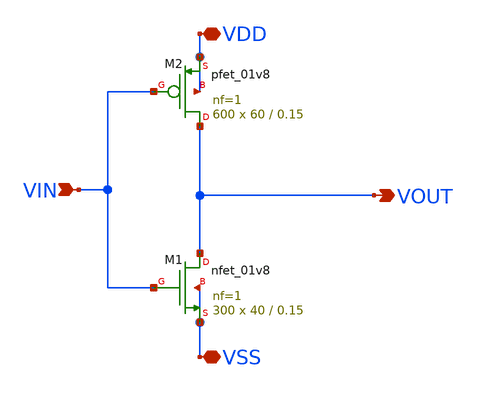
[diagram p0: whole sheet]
** sch_path: xschem/DC_DC_Converter_xschem/OTHERS/DC_DC_Converter_JV8/Inverter_4_v2/Inverter4_v2.sch
**.subckt Inverter4_v2 VIN VDD VSS VOUT
*.ipin VIN
*.iopin VDD
*.iopin VSS
*.opin VOUT
XM1 VOUT VIN VSS VSS sky130_fd_pr__nfet_01v8 L=0.15 W=40 nf=1 ad='int((nf+1)/2) * W/nf * 0.29' as='int((nf+2)/2) * W/nf * 0.29'
+ pd='2*int((nf+1)/2) * (W/nf + 0.29)' ps='2*int((nf+2)/2) * (W/nf + 0.29)' nrd='0.29 / W' nrs='0.29 / W'
+ sa=0 sb=0 sd=0 mult=300 m=300
XM2 VOUT VIN VDD VDD sky130_fd_pr__pfet_01v8 L=0.15 W=60 nf=1 ad='int((nf+1)/2) * W/nf * 0.29' as='int((nf+2)/2) * W/nf * 0.29'
+ pd='2*int((nf+1)/2) * (W/nf + 0.29)' ps='2*int((nf+2)/2) * (W/nf + 0.29)' nrd='0.29 / W' nrs='0.29 / W'
+ sa=0 sb=0 sd=0 mult=600 m=600
**.ends
.end
